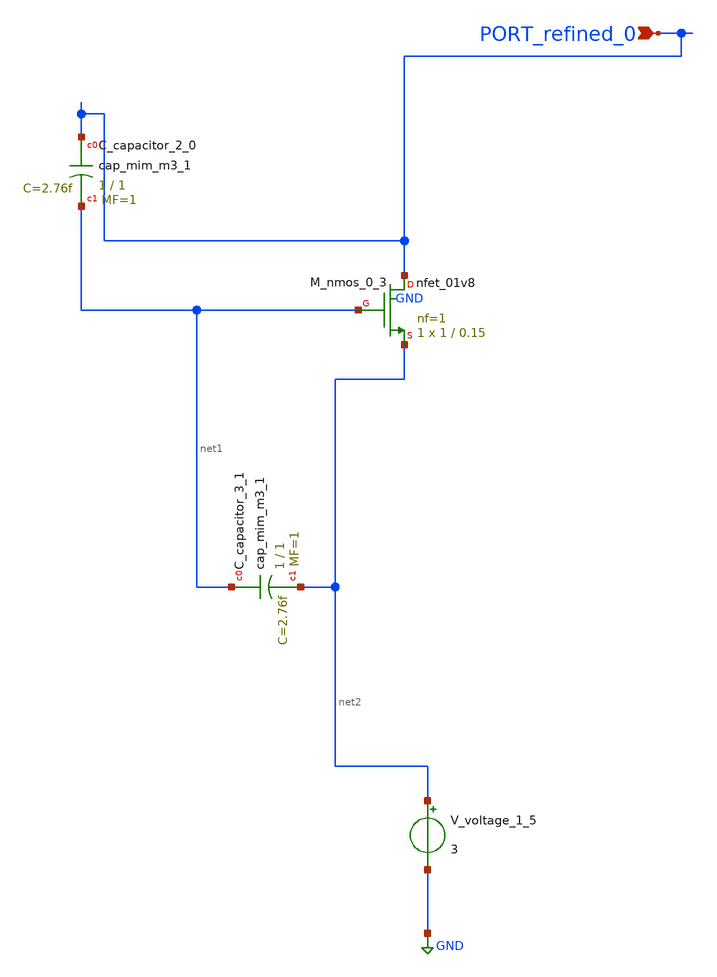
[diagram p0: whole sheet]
** sch_path: schematics/AMSNet/56.sch
**.subckt 56 PORT_refined_0
*.ipin PORT_refined_0
XC_capacitor_2_0 PORT_refined_0 net1 sky130_fd_pr__cap_mim_m3_1 W=1 L=1 MF=1 m=1
XC_capacitor_3_1 net1 net2 sky130_fd_pr__cap_mim_m3_1 W=1 L=1 MF=1 m=1
XM_nmos_0_3 PORT_refined_0 net1 net2 GND sky130_fd_pr__nfet_01v8 L=0.15 W=1 nf=1 ad='int((1 + 1)/2) * 1 / 1 * 0.29'
+ as='int((1 + 2)/2) * 1 / 1 * 0.29' pd='2*int((1 + 1)/2) * (1 / 1 + 0.29)' ps='2*int((1 + 2)/2) * (1 / 1 + 0.29)'
+ nrd='0.29 / 1 ' nrs='0.29 / 1 ' sa=0 sb=0 sd=0 mult=1 m=1
V_voltage_1_5 net2 GND 3
**.ends
.GLOBAL GND
.end
